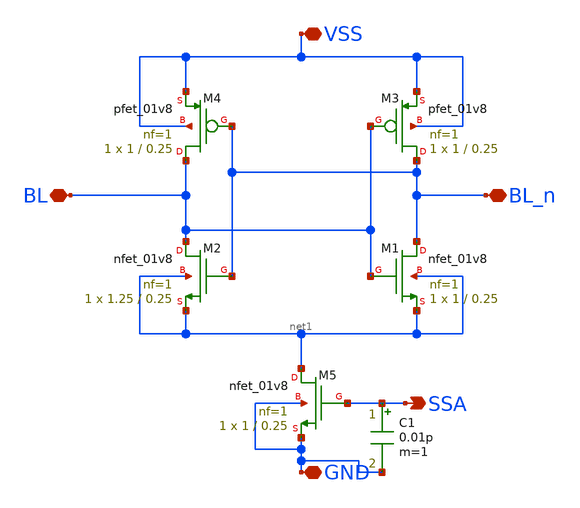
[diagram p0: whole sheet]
** sch_path: sense_amp.sch
**.subckt sense_amp VSS BL_n BL GND SSA
*.iopin VSS
*.iopin BL_n
*.iopin BL
*.iopin GND
*.opin SSA
XM1 BL_n BL net1 net1 sky130_fd_pr__nfet_01v8 L=0.25 W=1 nf=1 ad='int((nf+1)/2) * W/nf * 0.29' as='int((nf+2)/2) * W/nf * 0.29'
+ pd='2*int((nf+1)/2) * (W/nf + 0.29)' ps='2*int((nf+2)/2) * (W/nf + 0.29)' nrd='0.29 / W' nrs='0.29 / W'
+ sa=0 sb=0 sd=0 mult=1 m=1
XM2 BL BL_n net1 net1 sky130_fd_pr__nfet_01v8 L=0.25 W=1.25 nf=1 ad='int((nf+1)/2) * W/nf * 0.29' as='int((nf+2)/2) * W/nf * 0.29'
+ pd='2*int((nf+1)/2) * (W/nf + 0.29)' ps='2*int((nf+2)/2) * (W/nf + 0.29)' nrd='0.29 / W' nrs='0.29 / W'
+ sa=0 sb=0 sd=0 mult=1 m=1
XM3 BL_n BL VSS VSS sky130_fd_pr__pfet_01v8 L=0.25 W=1 nf=1 ad='int((nf+1)/2) * W/nf * 0.29' as='int((nf+2)/2) * W/nf * 0.29'
+ pd='2*int((nf+1)/2) * (W/nf + 0.29)' ps='2*int((nf+2)/2) * (W/nf + 0.29)' nrd='0.29 / W' nrs='0.29 / W'
+ sa=0 sb=0 sd=0 mult=1 m=1
XM4 BL BL_n VSS VSS sky130_fd_pr__pfet_01v8 L=0.25 W=1 nf=1 ad='int((nf+1)/2) * W/nf * 0.29' as='int((nf+2)/2) * W/nf * 0.29'
+ pd='2*int((nf+1)/2) * (W/nf + 0.29)' ps='2*int((nf+2)/2) * (W/nf + 0.29)' nrd='0.29 / W' nrs='0.29 / W'
+ sa=0 sb=0 sd=0 mult=1 m=1
XM5 net1 SSA GND GND sky130_fd_pr__nfet_01v8 L=0.25 W=1 nf=1 ad='int((nf+1)/2) * W/nf * 0.29' as='int((nf+2)/2) * W/nf * 0.29'
+ pd='2*int((nf+1)/2) * (W/nf + 0.29)' ps='2*int((nf+2)/2) * (W/nf + 0.29)' nrd='0.29 / W' nrs='0.29 / W'
+ sa=0 sb=0 sd=0 mult=1 m=1
C1 SSA GND 0.01p m=1
**.ends
.end
